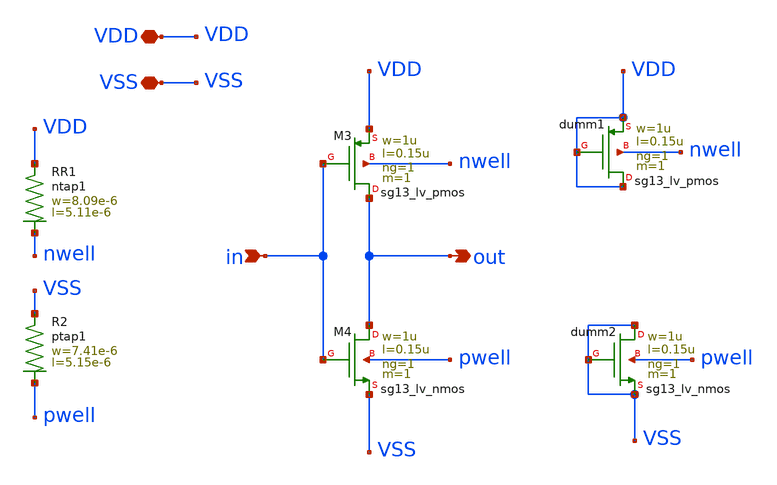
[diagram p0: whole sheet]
** sch_path: xschem/inv_lv.sch
**.subckt inv_lv in out VDD VSS
*.ipin in
*.opin out
*.iopin VDD
*.iopin VSS
XM3 out in VDD nwell sg13_lv_pmos w=1u l=0.15u ng=1 m=1 mm_ok=1
XM4 out in VSS pwell sg13_lv_nmos w=1u l=0.15u ng=1 m=1 mm_ok=1
Xdumm1 VDD VDD VDD nwell sg13_lv_pmos w=1u l=0.15u ng=1 m=1 mm_ok=1
Xdumm2 VSS VSS VSS pwell sg13_lv_nmos w=1u l=0.15u ng=1 m=1 mm_ok=1
XR1 VDD nwell ntap1 R=14.47 w=8.09e-6 l=5.11e-6
XR2 VSS pwell ptap1 R=15.49 w=7.41e-6 l=5.15e-6
**.ends
.end
